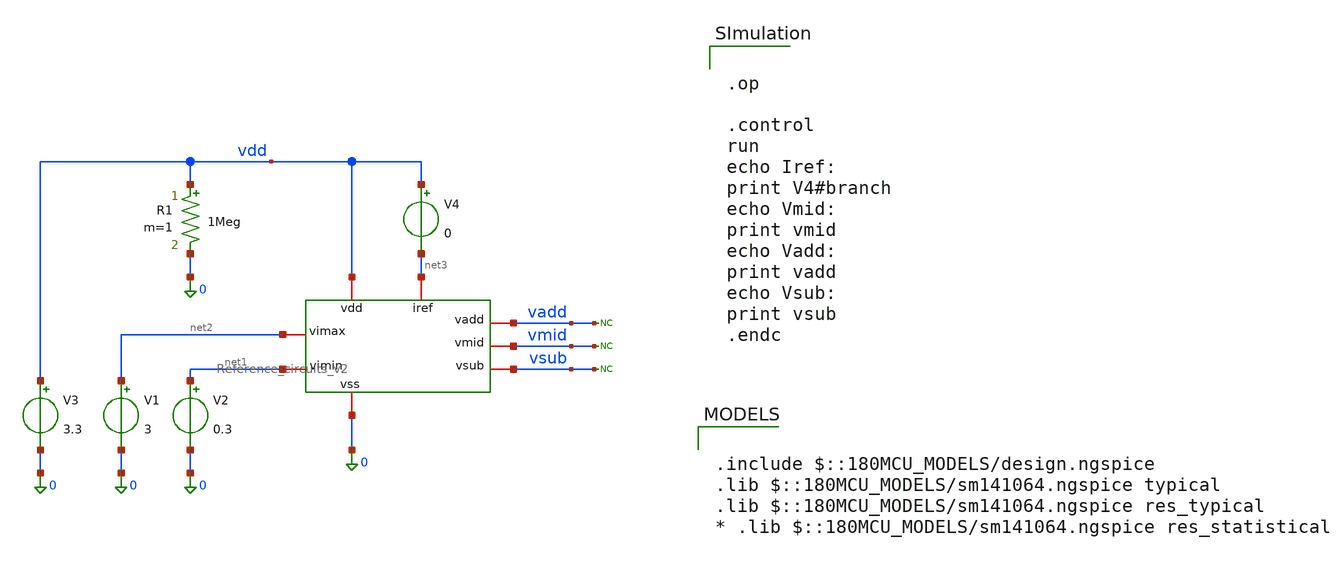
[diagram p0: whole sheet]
** sch_path: General/ADC/Reference/Reference_circuits_v2_tb.sch
**.subckt Reference_circuits_v2_tb
V1 net2 0 3
V2 net1 0 0.3
V3 vdd 0 3.3
* noconn vadd
* noconn vmid
* noconn vsub
R1 vdd 0 1Meg m=1
x1 net2 vadd net3 vmid 0 vsub net1 vdd Reference_circuits_v2
V4 vdd net3 0
**** begin user architecture code


.op

.control
run
echo Iref:
print V4#branch
echo Vmid:
print vmid
echo Vadd:
print vadd
echo Vsub:
print vsub
.endc



.include $::180MCU_MODELS/design.ngspice
.lib $::180MCU_MODELS/sm141064.ngspice typical
.lib $::180MCU_MODELS/sm141064.ngspice res_typical
* .lib $::180MCU_MODELS/sm141064.ngspice res_statistical

**** end user architecture code
**.ends

* expanding   symbol:  ADC/Reference/Reference_circuits_v2.sym # of pins=8
** sym_path: General/ADC/Reference/Reference_circuits_v2.sym
** sch_path: General/ADC/Reference/Reference_circuits_v2.sch
.subckt Reference_circuits_v2 vimax vadd iref vmid vss vsub vimin vdd
*.iopin vimax
*.iopin vimin
*.iopin iref
*.iopin vadd
*.iopin vmid
*.iopin vsub
*.iopin vss
*.iopin vdd
XR1 net1 vimax net1 nplus_u r_width=4e-6 r_length=500e-6 m=1
XR2 net2 net1 net2 nplus_u r_width=4e-6 r_length=500e-6 m=1
XR3 net3 net2 net3 nplus_u r_width=4e-6 r_length=500e-6 m=1
XR4 vimin net3 vimin nplus_u r_width=4e-6 r_length=500e-6 m=1
XM2 net4 net4 vimin vss nfet_03v3 L=2u W=20u nf=1 ad='int((nf+1)/2) * W/nf * 0.18u' as='int((nf+2)/2) * W/nf * 0.18u'
+ pd='2*int((nf+1)/2) * (W/nf + 0.18u)' ps='2*int((nf+2)/2) * (W/nf + 0.18u)' nrd='0.18u / W' nrs='0.18u / W'
+ sa=0 sb=0 sd=0 m=1
XR5 net4 vimax net4 ppolyf_u_2k r_width=5e-6 r_length=460e-6 m=1
XM1 iref net4 vimin vss nfet_03v3 L=2u W=2u nf=1 ad='int((nf+1)/2) * W/nf * 0.18u' as='int((nf+2)/2) * W/nf * 0.18u'
+ pd='2*int((nf+1)/2) * (W/nf + 0.18u)' ps='2*int((nf+2)/2) * (W/nf + 0.18u)' nrd='0.18u / W' nrs='0.18u / W'
+ sa=0 sb=0 sd=0 m=1
* noconn vdd
E1 vadd vss net1 vss 1
E2 vmid vss net2 vss 1
E3 vsub vss net3 vss 1
.ends

.end
